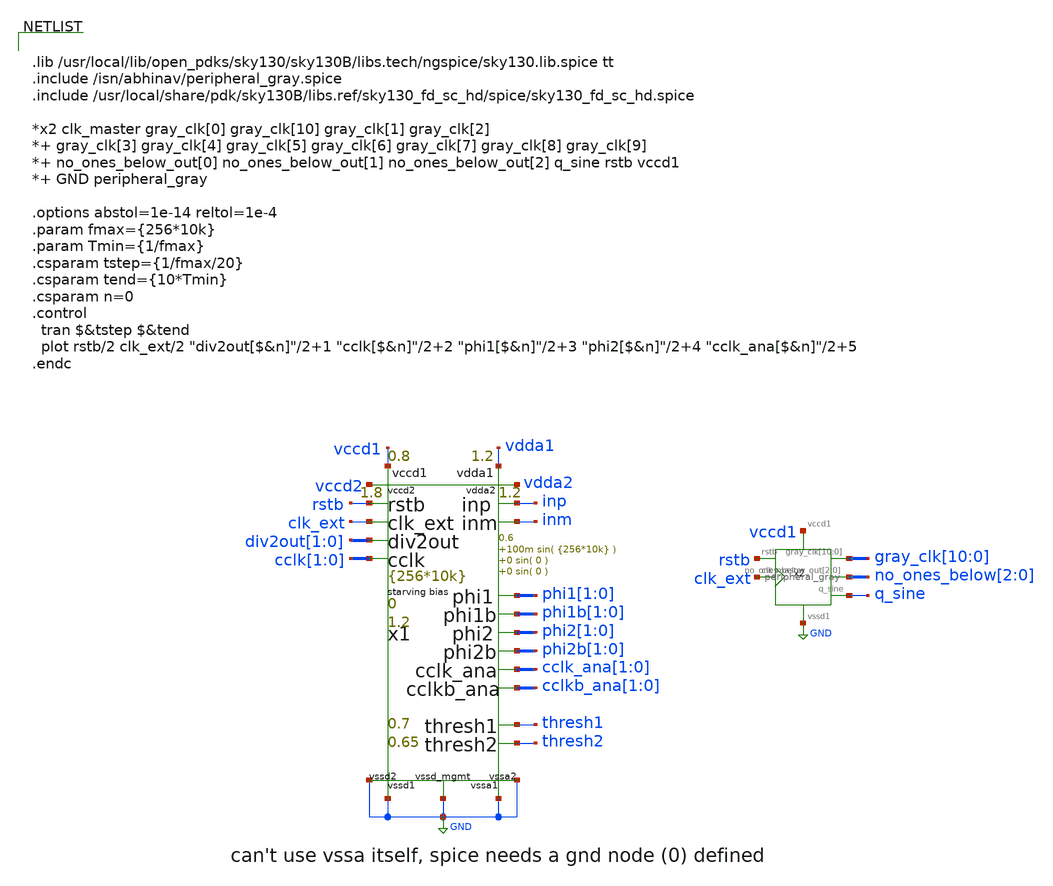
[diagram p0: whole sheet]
** sch_path: xschem/test_bench/peripheral_gray_tb.sch
**.subckt peripheral_gray_tb
x1 thresh1 thresh2 inp inm clk_ext rstb phi1[1] phi1[0] phi1b[1] phi1b[0] phi2[1] phi2[0] phi2b[1] phi2b[0]
+ cclk_ana[1] cclk_ana[0] cclkb_ana[1] cclkb_ana[0] div2out[1] div2out[0] cclk[1] cclk[0] vdda1 vccd1 vccd2
+ vdda2 GND GND GND GND GND risc_signals p_vdda1=1.2 p_vdda2=1.2 p_vccd1=0.8 p_vccd2=1.8 p_vccd_mgmt=1.8
+ p_fclk={256*10k} p_duty_cycle=0.5 p_rstb_delay={1.5/p_fclk} p_rstb_tr=5n p_thresh1=0.7 p_thresh2=0.65
+ p_vpb=0 p_vnb=1.2 p_vcm=0.6 p_amp1=100m p_f1={256*10k} p_amp2=0 p_f2=0 p_amp3=0 p_f3=0
x2 rstb gray_clk[10] gray_clk[9] gray_clk[8] gray_clk[7] gray_clk[6] gray_clk[5] gray_clk[4]
+ gray_clk[3] gray_clk[2] gray_clk[1] gray_clk[0] vccd1 GND clk_ext no_ones_below[2] no_ones_below[1]
+ no_ones_below[0] q_sine peripheral_gray
**** begin user architecture code


.lib /usr/local/lib/open_pdks/sky130/sky130B/libs.tech/ngspice/sky130.lib.spice tt
.include /isn/abhinav/peripheral_gray.spice
.include /usr/local/share/pdk/sky130B/libs.ref/sky130_fd_sc_hd/spice/sky130_fd_sc_hd.spice

*x2 clk_master gray_clk[0] gray_clk[10] gray_clk[1] gray_clk[2]
*+ gray_clk[3] gray_clk[4] gray_clk[5] gray_clk[6] gray_clk[7] gray_clk[8] gray_clk[9]
*+ no_ones_below_out[0] no_ones_below_out[1] no_ones_below_out[2] q_sine rstb vccd1
*+ GND peripheral_gray

.options abstol=1e-14 reltol=1e-4
.param fmax={256*10k}
.param Tmin={1/fmax}
.csparam tstep={1/fmax/20}
.csparam tend={10*Tmin}
.csparam n=0
.control
  tran $&tstep $&tend
  plot rstb/2 clk_ext/2 "div2out[$&n]"/2+1 "cclk[$&n]"/2+2 "phi1[$&n]"/2+3 "phi2[$&n]"/2+4
+ "cclk_ana[$&n]"/2+5
.endc


**** end user architecture code
**.ends
.GLOBAL GND
.end
